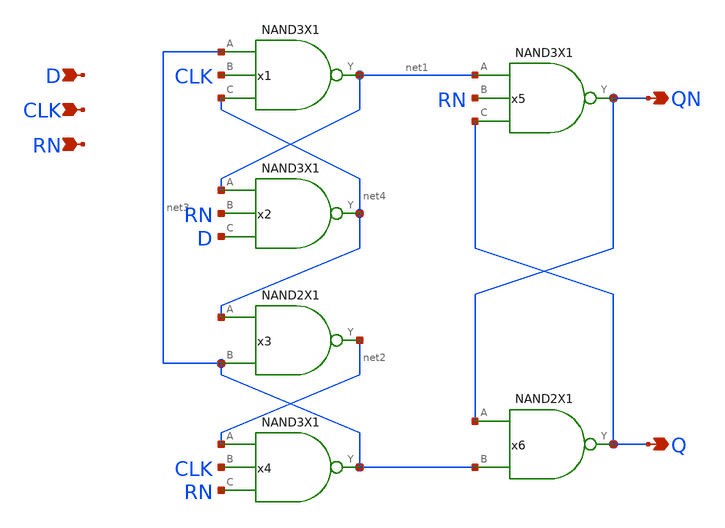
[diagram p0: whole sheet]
** sch_path: lib/xschem/DFFRNX1.sch
**.subckt DFFRNX1 Q QN D CLK RN
*.opin Q
*.opin QN
*.ipin D
*.ipin CLK
*.ipin RN
x2 net4 net1 RN D NAND3X1
x1 net1 net3 CLK net4 NAND3X1
x3 net2 net4 net3 NAND2X1
x4 net3 net2 CLK RN NAND3X1
x5 QN net1 RN Q NAND3X1
x6 Q QN net3 NAND2X1
**.ends
.end
